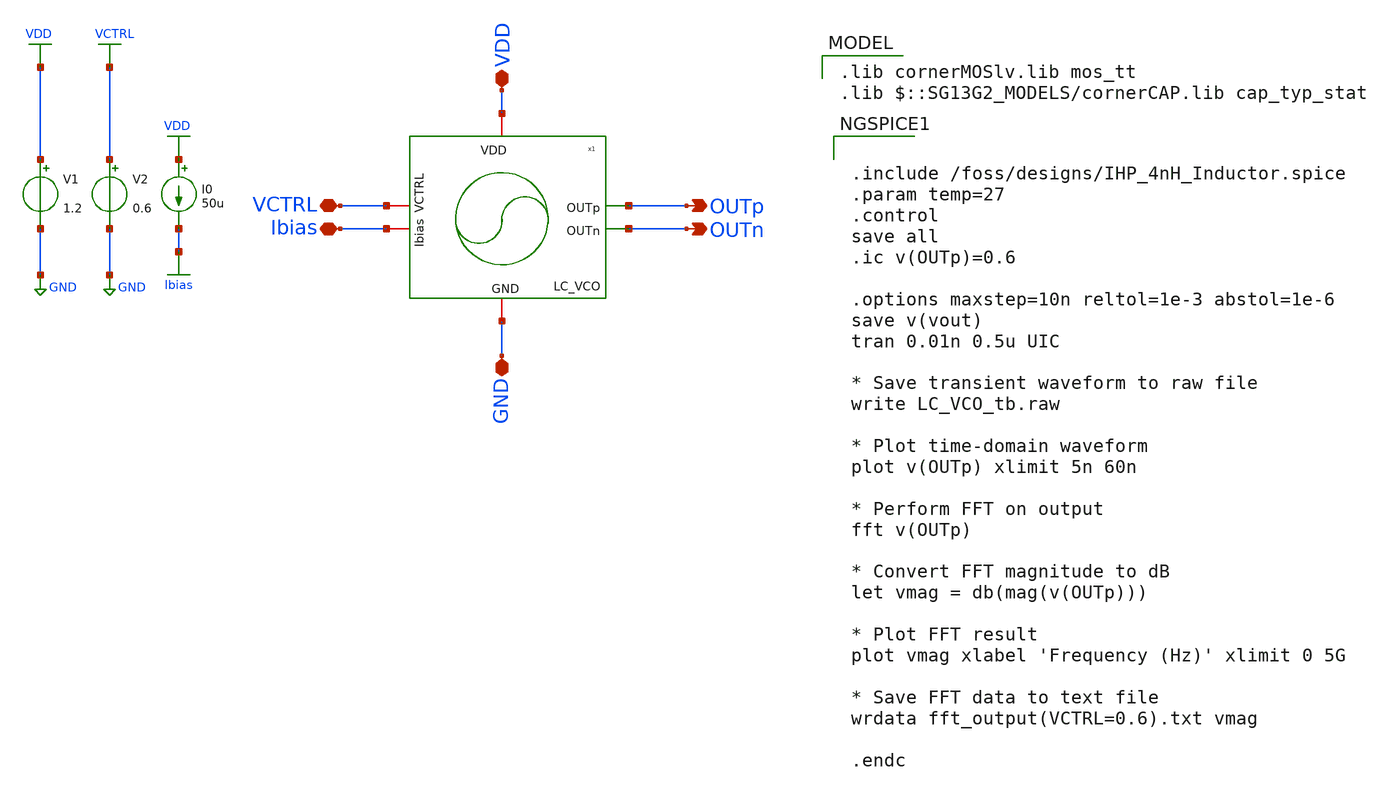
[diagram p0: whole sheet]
** sch_path: schematic/blocks/lc-vco/LC_VCO_tb.sch
**.subckt LC_VCO_tb OUTp OUTn VDD VCTRL GND Ibias
*.opin OUTp
*.opin OUTn
*.iopin VDD
*.iopin VCTRL
*.iopin GND
*.iopin Ibias
V1 VDD GND 1.2
V2 VCTRL GND 0.6
x1 VDD OUTp OUTn Ibias VCTRL GND LC_VCO
I0 VDD Ibias 50u
**** begin user architecture code
 .lib cornerMOSlv.lib mos_tt
.lib $::SG13G2_MODELS/cornerCAP.lib cap_typ_stat



.include /foss/designs/IHP_4nH_Inductor.spice
.param temp=27
.control
save all
.ic v(OUTp)=0.6

.options maxstep=10n reltol=1e-3 abstol=1e-6
save v(vout)
tran 0.01n 0.5u UIC

* Save transient waveform to raw file
write LC_VCO_tb.raw

* Plot time-domain waveform
plot v(OUTp) xlimit 5n 60n

* Perform FFT on output
fft v(OUTp)

* Convert FFT magnitude to dB
let vmag = db(mag(v(OUTp)))

* Plot FFT result
plot vmag xlabel 'Frequency (Hz)' xlimit 0 5G

* Save FFT data to text file
wrdata fft_output(VCTRL=0.6).txt vmag

.endc


**** end user architecture code
**.ends

* expanding   symbol:  LC_VCO.sym # of pins=6
** sym_path: LC_VCO.sym
** sch_path: LC_VCO.sch
.subckt LC_VCO VDD OUTp OUTn Ibias VCTRL GND
*.iopin VDD
*.opin OUTp
*.opin OUTn
*.iopin GND
*.iopin VCTRL
*.iopin Ibias
XM6 net1 Ibias GND GND sg13_lv_nmos w=1u l=0.15u ng=1 m=60 mm_ok=1
XM5 Ibias Ibias GND GND sg13_lv_nmos w=1u l=0.15u ng=1 m=1 mm_ok=1
XM4 OUTp OUTn VDD VDD sg13_lv_pmos w=8.5u l=0.5u ng=1 m=13 mm_ok=1
X5M3 OUTn OUTp VDD VDD sg13_lv_pmos w=8.5u l=0.5u ng=1 m=13 mm_ok=1
XM2 OUTp OUTn net1 GND sg13_lv_nmos w=2u l=0.5u ng=1 m=12 mm_ok=1
XM1 OUTn OUTp net1 GND sg13_lv_nmos w=2u l=0.5u ng=1 m=12 mm_ok=1
XC3 OUTp OUTn cap_cmim w=4.0e-6 l=4.0e-6 m=13.6 mm_ok=1
XMv2 OUTp VCTRL OUTp VDD sg13_lv_pmos w=4u l=4u ng=1 m=22 mm_ok=1
XMv1 OUTn VCTRL OUTn VDD sg13_lv_pmos w=4u l=4u ng=1 m=22 mm_ok=1
XR1 OUTp OUTn sub! rhigh w=1e-6 l=1e-6 m=1.23 b=0 mm_ok=1
x1 OUTn OUTp ihp_4nh_inductor
.ends

.GLOBAL GND
.GLOBAL VDD
.GLOBAL VCTRL
.GLOBAL Ibias
.end
